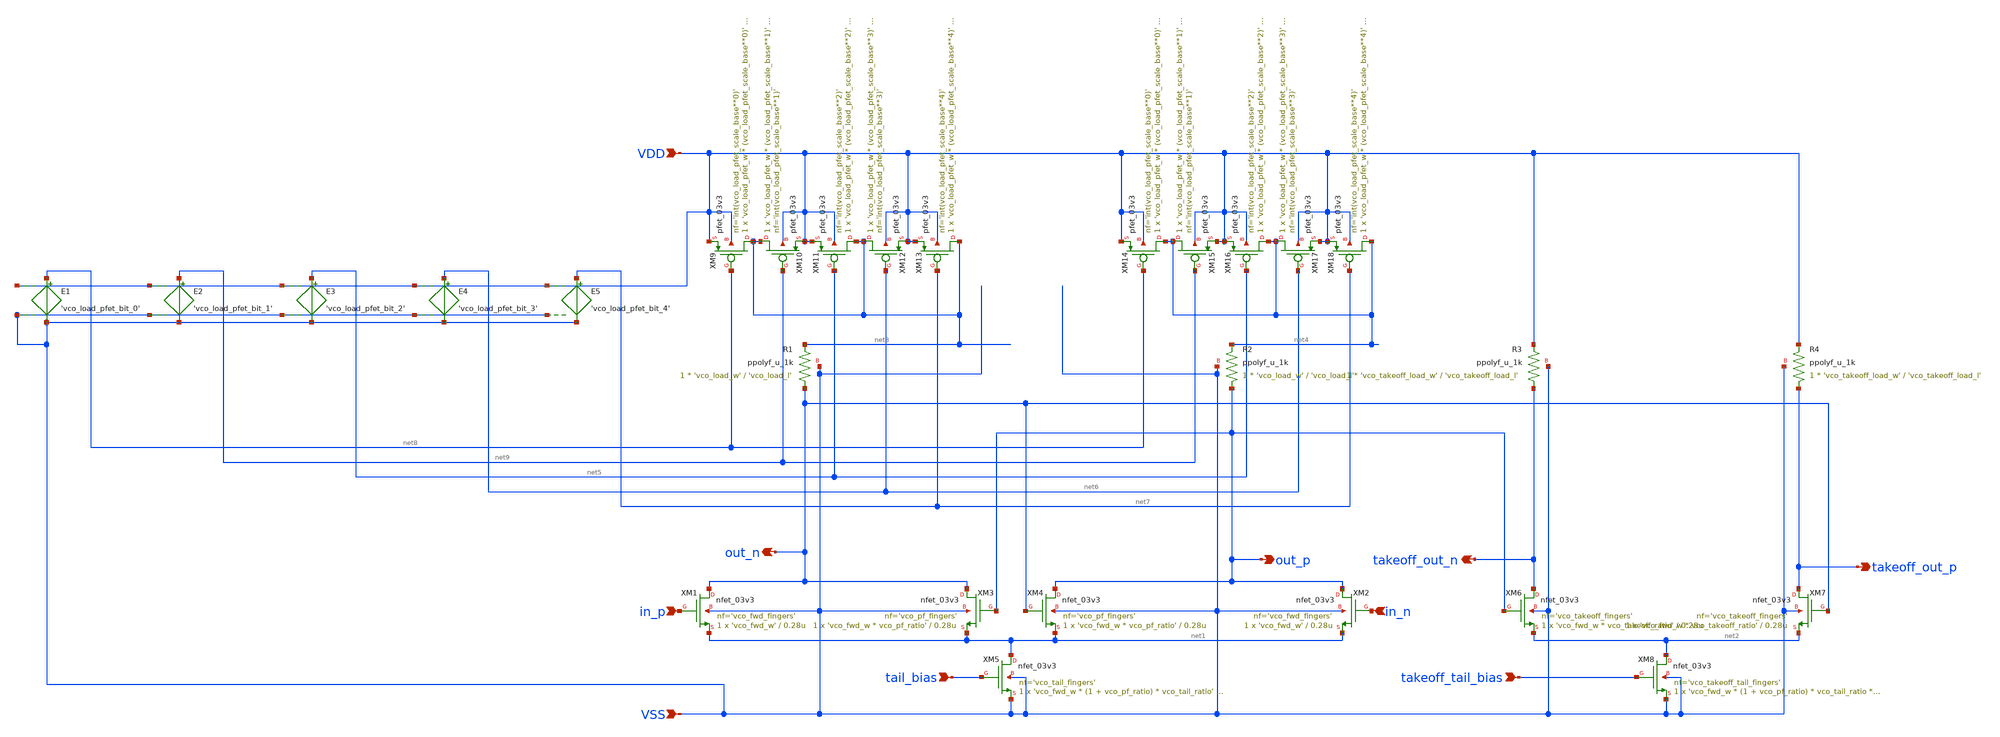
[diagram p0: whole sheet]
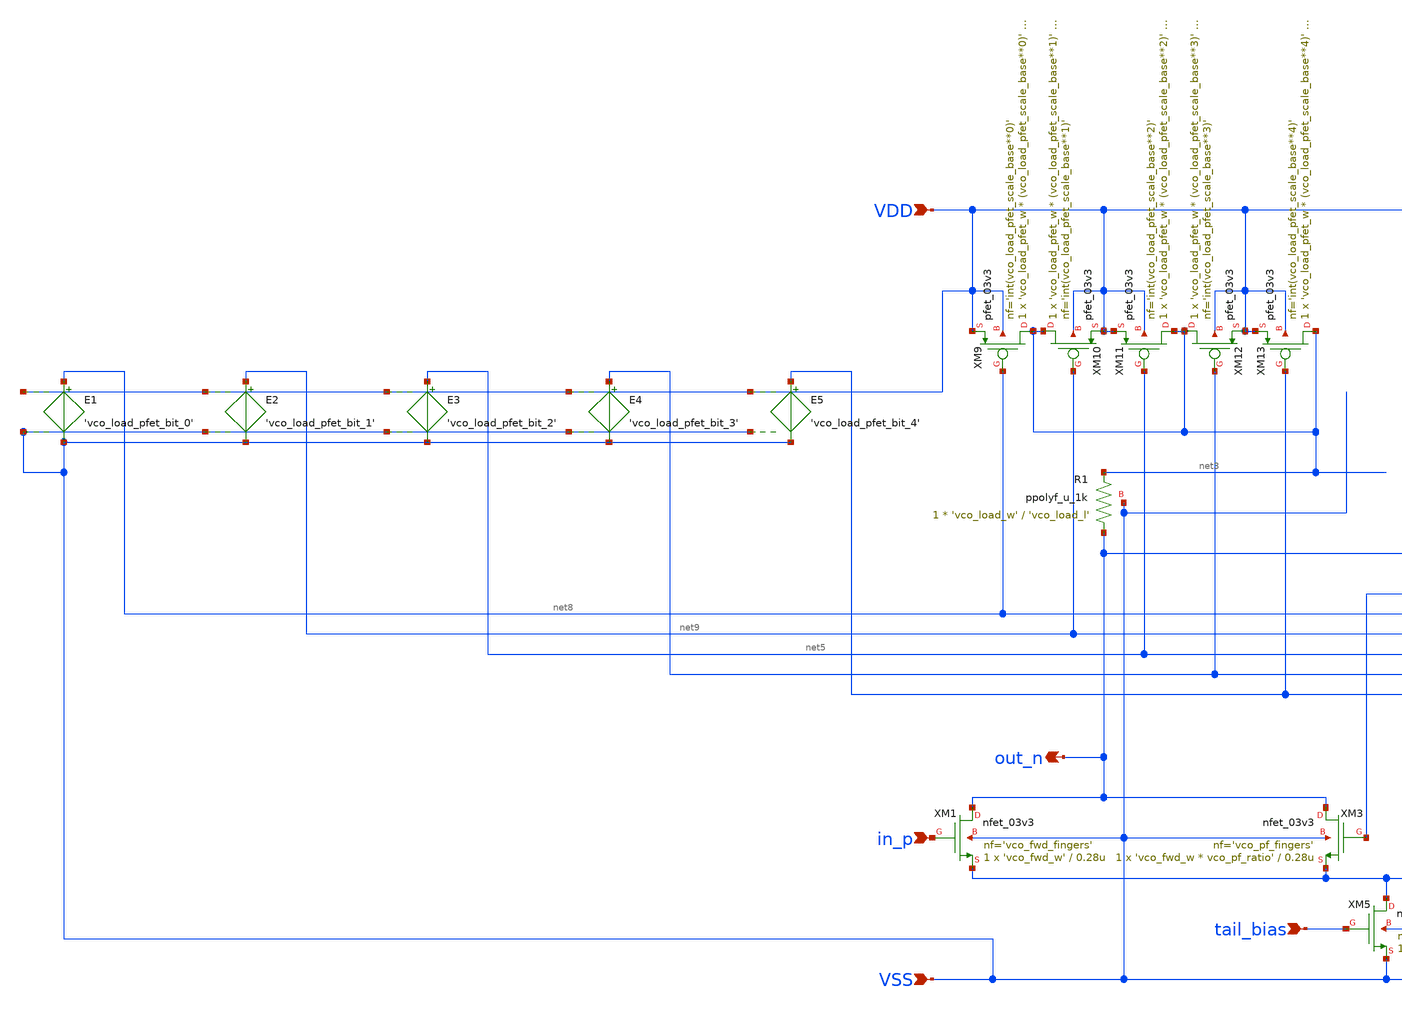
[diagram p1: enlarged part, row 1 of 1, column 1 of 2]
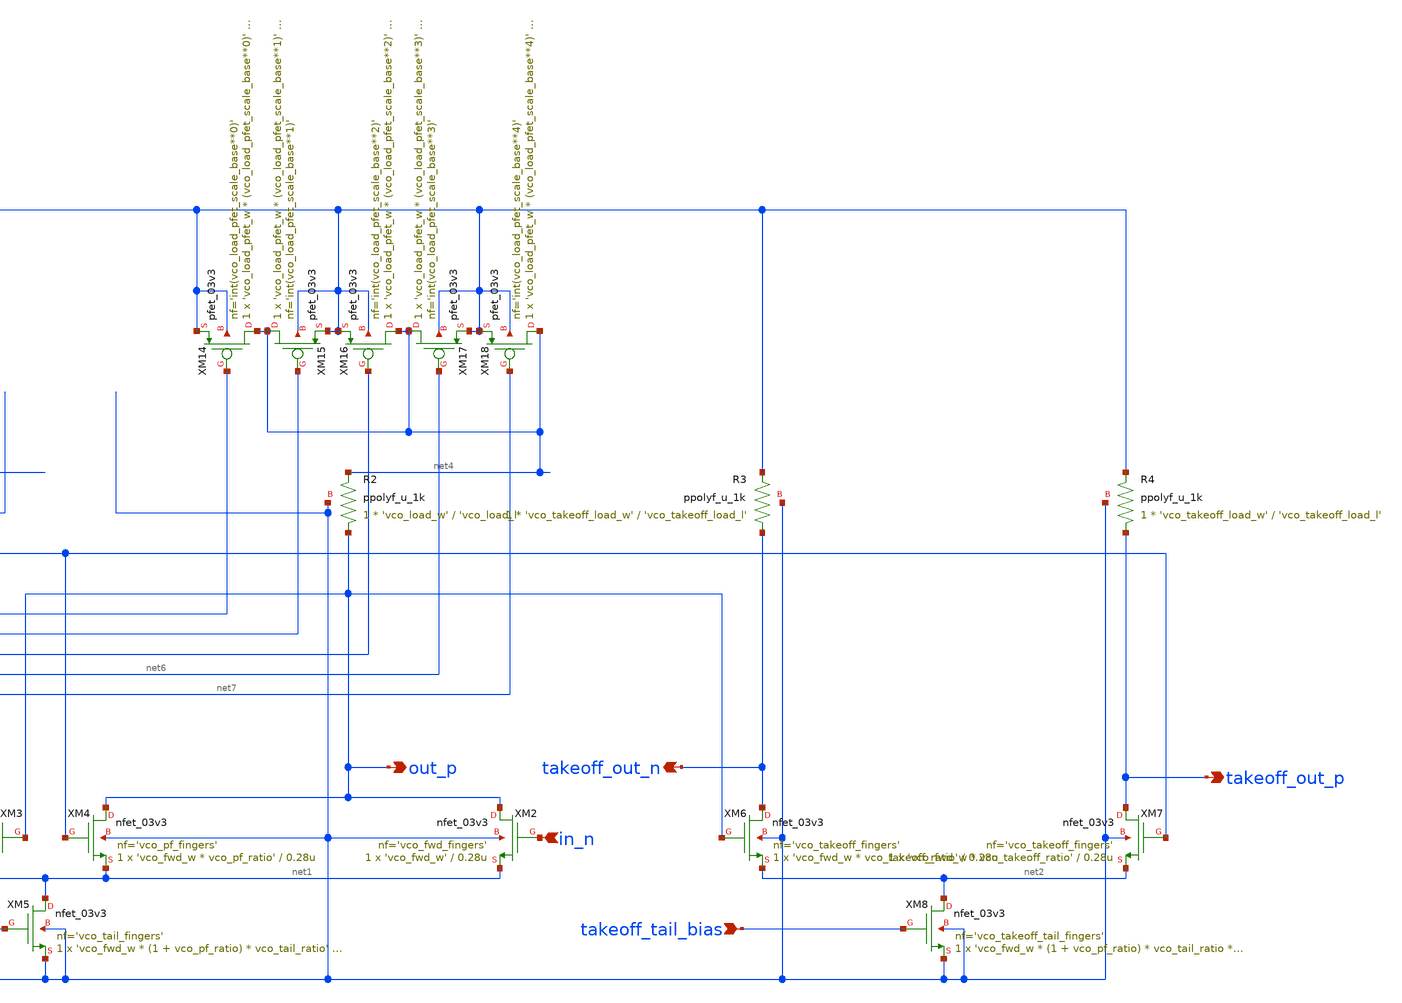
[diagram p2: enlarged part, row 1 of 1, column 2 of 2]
** sch_path: xschem/vco_core_segment.sch
**.subckt vco_core_segment VSS VDD out_n out_p in_p in_n takeoff_out_n takeoff_out_p tail_bias
*+ takeoff_tail_bias
*.ipin VSS
*.ipin VDD
*.opin out_n
*.opin out_p
*.ipin in_p
*.ipin in_n
*.opin takeoff_out_n
*.opin takeoff_out_p
*.ipin tail_bias
*.ipin takeoff_tail_bias
XM1 out_n in_p net1 VSS nfet_03v3 L=0.28u W='vco_fwd_w' nf='vco_fwd_fingers' ad='int((nf+1)/2) * W/nf * 0.18u'
+ as='int((nf+2)/2) * W/nf * 0.18u' pd='2*int((nf+1)/2) * (W/nf + 0.18u)' ps='2*int((nf+2)/2) * (W/nf + 0.18u)'
+ nrd='0.18u / W' nrs='0.18u / W' sa=0 sb=0 sd=0 m=1
XM3 out_n out_p net1 VSS nfet_03v3 L=0.28u W='vco_fwd_w * vco_pf_ratio' nf='vco_pf_fingers' ad='int((nf+1)/2) * W/nf * 0.18u'
+ as='int((nf+2)/2) * W/nf * 0.18u' pd='2*int((nf+1)/2) * (W/nf + 0.18u)' ps='2*int((nf+2)/2) * (W/nf + 0.18u)'
+ nrd='0.18u / W' nrs='0.18u / W' sa=0 sb=0 sd=0 m=1
XM4 out_p out_n net1 VSS nfet_03v3 L=0.28u W='vco_fwd_w * vco_pf_ratio' nf='vco_pf_fingers' ad='int((nf+1)/2) * W/nf * 0.18u'
+ as='int((nf+2)/2) * W/nf * 0.18u' pd='2*int((nf+1)/2) * (W/nf + 0.18u)' ps='2*int((nf+2)/2) * (W/nf + 0.18u)'
+ nrd='0.18u / W' nrs='0.18u / W' sa=0 sb=0 sd=0 m=1
XM5 net1 tail_bias VSS VSS nfet_03v3 L='vco_tail_l' W='vco_fwd_w * (1 + vco_pf_ratio) * vco_tail_ratio'
+ nf='vco_tail_fingers' ad='int((nf+1)/2) * W/nf * 0.18u' as='int((nf+2)/2) * W/nf * 0.18u' pd='2*int((nf+1)/2) * (W/nf + 0.18u)'
+ ps='2*int((nf+2)/2) * (W/nf + 0.18u)' nrd='0.18u / W' nrs='0.18u / W' sa=0 sb=0 sd=0 m=1
XM2 out_p in_n net1 VSS nfet_03v3 L=0.28u W='vco_fwd_w' nf='vco_fwd_fingers' ad='int((nf+1)/2) * W/nf * 0.18u'
+ as='int((nf+2)/2) * W/nf * 0.18u' pd='2*int((nf+1)/2) * (W/nf + 0.18u)' ps='2*int((nf+2)/2) * (W/nf + 0.18u)'
+ nrd='0.18u / W' nrs='0.18u / W' sa=0 sb=0 sd=0 m=1
XR1 out_n net3 VSS ppolyf_u_1k r_width='vco_load_w' r_length='vco_load_l' m=1
XR2 out_p net4 VSS ppolyf_u_1k r_width='vco_load_w' r_length='vco_load_l' m=1
XM6 takeoff_out_n out_p net2 VSS nfet_03v3 L=0.28u W='vco_fwd_w * vco_takeoff_ratio' nf='vco_takeoff_fingers'
+ ad='int((nf+1)/2) * W/nf * 0.18u' as='int((nf+2)/2) * W/nf * 0.18u' pd='2*int((nf+1)/2) * (W/nf + 0.18u)'
+ ps='2*int((nf+2)/2) * (W/nf + 0.18u)' nrd='0.18u / W' nrs='0.18u / W' sa=0 sb=0 sd=0 m=1
XM7 takeoff_out_p out_n net2 VSS nfet_03v3 L=0.28u W='vco_fwd_w * vco_takeoff_ratio' nf='vco_takeoff_fingers'
+ ad='int((nf+1)/2) * W/nf * 0.18u' as='int((nf+2)/2) * W/nf * 0.18u' pd='2*int((nf+1)/2) * (W/nf + 0.18u)'
+ ps='2*int((nf+2)/2) * (W/nf + 0.18u)' nrd='0.18u / W' nrs='0.18u / W' sa=0 sb=0 sd=0 m=1
XM8 net2 takeoff_tail_bias VSS VSS nfet_03v3 L='vco_takeoff_tail_l' W='vco_fwd_w * (1 + vco_pf_ratio) * vco_tail_ratio * vco_takeoff_ratio'
+ nf='vco_takeoff_tail_fingers' ad='int((nf+1)/2) * W/nf * 0.18u' as='int((nf+2)/2) * W/nf * 0.18u' pd='2*int((nf+1)/2) * (W/nf + 0.18u)'
+ ps='2*int((nf+2)/2) * (W/nf + 0.18u)' nrd='0.18u / W' nrs='0.18u / W' sa=0 sb=0 sd=0 m=1
XR3 takeoff_out_n VDD VSS ppolyf_u_1k r_width='vco_takeoff_load_w' r_length='vco_takeoff_load_l' m=1
XR4 takeoff_out_p VDD VSS ppolyf_u_1k r_width='vco_takeoff_load_w' r_length='vco_takeoff_load_l' m=1
XM9 net3 net8 VDD VDD pfet_03v3 L='vco_load_pfet_l' W='vco_load_pfet_w * (vco_load_pfet_scale_base**0)'
+ nf='int(vco_load_pfet_scale_base**0)' ad='int((nf+1)/2) * W/nf * 0.18u' as='int((nf+2)/2) * W/nf * 0.18u'
+ pd='2*int((nf+1)/2) * (W/nf + 0.18u)' ps='2*int((nf+2)/2) * (W/nf + 0.18u)' nrd='0.18u / W' nrs='0.18u / W'
+ sa=0 sb=0 sd=0 m=1
XM10 net3 net9 VDD VDD pfet_03v3 L='vco_load_pfet_l' W='vco_load_pfet_w * (vco_load_pfet_scale_base**1)'
+ nf='int(vco_load_pfet_scale_base**1)' ad='int((nf+1)/2) * W/nf * 0.18u' as='int((nf+2)/2) * W/nf * 0.18u'
+ pd='2*int((nf+1)/2) * (W/nf + 0.18u)' ps='2*int((nf+2)/2) * (W/nf + 0.18u)' nrd='0.18u / W' nrs='0.18u / W'
+ sa=0 sb=0 sd=0 m=1
XM11 net3 net5 VDD VDD pfet_03v3 L='vco_load_pfet_l' W='vco_load_pfet_w * (vco_load_pfet_scale_base**2)'
+ nf='int(vco_load_pfet_scale_base**2)' ad='int((nf+1)/2) * W/nf * 0.18u' as='int((nf+2)/2) * W/nf * 0.18u'
+ pd='2*int((nf+1)/2) * (W/nf + 0.18u)' ps='2*int((nf+2)/2) * (W/nf + 0.18u)' nrd='0.18u / W' nrs='0.18u / W'
+ sa=0 sb=0 sd=0 m=1
XM12 net3 net6 VDD VDD pfet_03v3 L='vco_load_pfet_l' W='vco_load_pfet_w * (vco_load_pfet_scale_base**3)'
+ nf='int(vco_load_pfet_scale_base**3)' ad='int((nf+1)/2) * W/nf * 0.18u' as='int((nf+2)/2) * W/nf * 0.18u'
+ pd='2*int((nf+1)/2) * (W/nf + 0.18u)' ps='2*int((nf+2)/2) * (W/nf + 0.18u)' nrd='0.18u / W' nrs='0.18u / W'
+ sa=0 sb=0 sd=0 m=1
XM13 net3 net7 VDD VDD pfet_03v3 L='vco_load_pfet_l' W='vco_load_pfet_w * (vco_load_pfet_scale_base**4)'
+ nf='int(vco_load_pfet_scale_base**4)' ad='int((nf+1)/2) * W/nf * 0.18u' as='int((nf+2)/2) * W/nf * 0.18u'
+ pd='2*int((nf+1)/2) * (W/nf + 0.18u)' ps='2*int((nf+2)/2) * (W/nf + 0.18u)' nrd='0.18u / W' nrs='0.18u / W'
+ sa=0 sb=0 sd=0 m=1
XM14 net4 net8 VDD VDD pfet_03v3 L='vco_load_pfet_l' W='vco_load_pfet_w * (vco_load_pfet_scale_base**0)'
+ nf='int(vco_load_pfet_scale_base**0)' ad='int((nf+1)/2) * W/nf * 0.18u' as='int((nf+2)/2) * W/nf * 0.18u'
+ pd='2*int((nf+1)/2) * (W/nf + 0.18u)' ps='2*int((nf+2)/2) * (W/nf + 0.18u)' nrd='0.18u / W' nrs='0.18u / W'
+ sa=0 sb=0 sd=0 m=1
XM15 net4 net9 VDD VDD pfet_03v3 L='vco_load_pfet_l' W='vco_load_pfet_w * (vco_load_pfet_scale_base**1)'
+ nf='int(vco_load_pfet_scale_base**1)' ad='int((nf+1)/2) * W/nf * 0.18u' as='int((nf+2)/2) * W/nf * 0.18u'
+ pd='2*int((nf+1)/2) * (W/nf + 0.18u)' ps='2*int((nf+2)/2) * (W/nf + 0.18u)' nrd='0.18u / W' nrs='0.18u / W'
+ sa=0 sb=0 sd=0 m=1
XM16 net4 net5 VDD VDD pfet_03v3 L='vco_load_pfet_l' W='vco_load_pfet_w * (vco_load_pfet_scale_base**2)'
+ nf='int(vco_load_pfet_scale_base**2)' ad='int((nf+1)/2) * W/nf * 0.18u' as='int((nf+2)/2) * W/nf * 0.18u'
+ pd='2*int((nf+1)/2) * (W/nf + 0.18u)' ps='2*int((nf+2)/2) * (W/nf + 0.18u)' nrd='0.18u / W' nrs='0.18u / W'
+ sa=0 sb=0 sd=0 m=1
XM17 net4 net6 VDD VDD pfet_03v3 L='vco_load_pfet_l' W='vco_load_pfet_w * (vco_load_pfet_scale_base**3)'
+ nf='int(vco_load_pfet_scale_base**3)' ad='int((nf+1)/2) * W/nf * 0.18u' as='int((nf+2)/2) * W/nf * 0.18u'
+ pd='2*int((nf+1)/2) * (W/nf + 0.18u)' ps='2*int((nf+2)/2) * (W/nf + 0.18u)' nrd='0.18u / W' nrs='0.18u / W'
+ sa=0 sb=0 sd=0 m=1
XM18 net4 net7 VDD VDD pfet_03v3 L='vco_load_pfet_l' W='vco_load_pfet_w * (vco_load_pfet_scale_base**4)'
+ nf='int(vco_load_pfet_scale_base**4)' ad='int((nf+1)/2) * W/nf * 0.18u' as='int((nf+2)/2) * W/nf * 0.18u'
+ pd='2*int((nf+1)/2) * (W/nf + 0.18u)' ps='2*int((nf+2)/2) * (W/nf + 0.18u)' nrd='0.18u / W' nrs='0.18u / W'
+ sa=0 sb=0 sd=0 m=1
E1 net8 VSS VDD VSS 'vco_load_pfet_bit_0'
E2 net9 VSS VDD VSS 'vco_load_pfet_bit_1'
E3 net5 VSS VDD VSS 'vco_load_pfet_bit_2'
E4 net6 VSS VDD VSS 'vco_load_pfet_bit_3'
E5 net7 VSS VDD VSS 'vco_load_pfet_bit_4'
**.ends
.end
